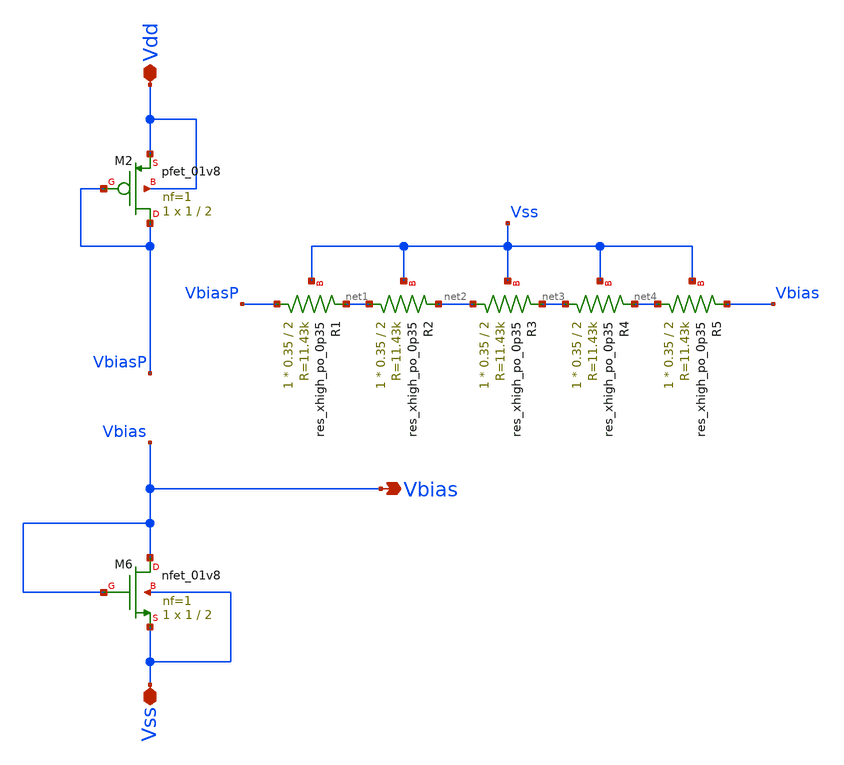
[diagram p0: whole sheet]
** sch_path: Circuits/Examples/MillerOpAmpCMMFB/Bias.sch
**.subckt Bias Vbias Vss Vdd
*.opin Vbias
*.iopin Vss
*.iopin Vdd
XM6 Vbias Vbias Vss Vss sky130_fd_pr__nfet_01v8 L=2 W=1 nf=1 ad='int((nf+1)/2) * W/nf * 0.29' as='int((nf+2)/2) * W/nf * 0.29'
+ pd='2*int((nf+1)/2) * (W/nf + 0.29)' ps='2*int((nf+2)/2) * (W/nf + 0.29)' nrd='0.29 / W' nrs='0.29 / W'
+ sa=0 sb=0 sd=0 mult=1 m=1
XM2 VbiasP VbiasP Vdd Vdd sky130_fd_pr__pfet_01v8 L=2 W=1 nf=1 ad='int((nf+1)/2) * W/nf * 0.29' as='int((nf+2)/2) * W/nf * 0.29'
+ pd='2*int((nf+1)/2) * (W/nf + 0.29)' ps='2*int((nf+2)/2) * (W/nf + 0.29)' nrd='0.29 / W' nrs='0.29 / W'
+ sa=0 sb=0 sd=0 mult=1 m=1
XR1 VbiasP net1 Vss sky130_fd_pr__res_xhigh_po_0p35 L=2 mult=1 m=1
XR2 net1 net2 Vss sky130_fd_pr__res_xhigh_po_0p35 L=2 mult=1 m=1
XR3 net2 net3 Vss sky130_fd_pr__res_xhigh_po_0p35 L=2 mult=1 m=1
XR4 net3 net4 Vss sky130_fd_pr__res_xhigh_po_0p35 L=2 mult=1 m=1
XR5 net4 Vbias Vss sky130_fd_pr__res_xhigh_po_0p35 L=2 mult=1 m=1
**.ends
.end
